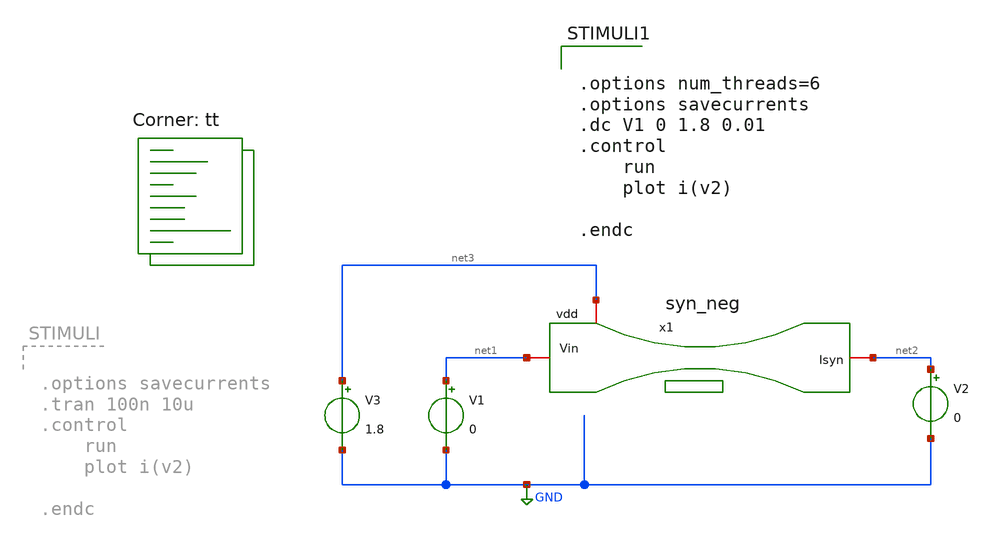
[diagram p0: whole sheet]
** sch_path: Neuron/ultralif/tb_syn_neg.sch
**.subckt tb_syn_neg
V1 net1 GND 0
V2 net2 GND 0
V3 net3 GND 1.8
x1 net3 net1 net2 syn_neg
**** begin user architecture code
.lib $::SKYWATER_MODELS/sky130.lib.spice tt
**** end user architecture code
**.ends

* expanding   symbol:  syn_neg.sym # of pins=3
** sym_path: Neuron/ultralif/syn_neg.sym
** sch_path: Neuron/ultralif/syn_neg.sch
.subckt syn_neg vdd Vin Isyn
*.iopin Vin
*.iopin Isyn
*.iopin vdd
XM10 Isyn Vin vx vdd sky130_fd_pr__pfet_01v8 L=30 W=0.5 nf=1 ad='int((nf+1)/2) * W/nf * 0.29' as='int((nf+2)/2) * W/nf * 0.29'
+ pd='2*int((nf+1)/2) * (W/nf + 0.29)' ps='2*int((nf+2)/2) * (W/nf + 0.29)' nrd='0.29 / W' nrs='0.29 / W'
+ sa=0 sb=0 sd=0 mult=1 m=1
XM1 vx Vin vdd vdd sky130_fd_pr__pfet_01v8 L=30 W=0.5 nf=1 ad='int((nf+1)/2) * W/nf * 0.29' as='int((nf+2)/2) * W/nf * 0.29'
+ pd='2*int((nf+1)/2) * (W/nf + 0.29)' ps='2*int((nf+2)/2) * (W/nf + 0.29)' nrd='0.29 / W' nrs='0.29 / W'
+ sa=0 sb=0 sd=0 mult=1 m=1
.ends

.GLOBAL GND
**** begin user architecture code


.options num_threads=6
.options savecurrents
.dc V1 0 1.8 0.01
.control
	run
	plot i(v2)

.endc


**** end user architecture code
.end
